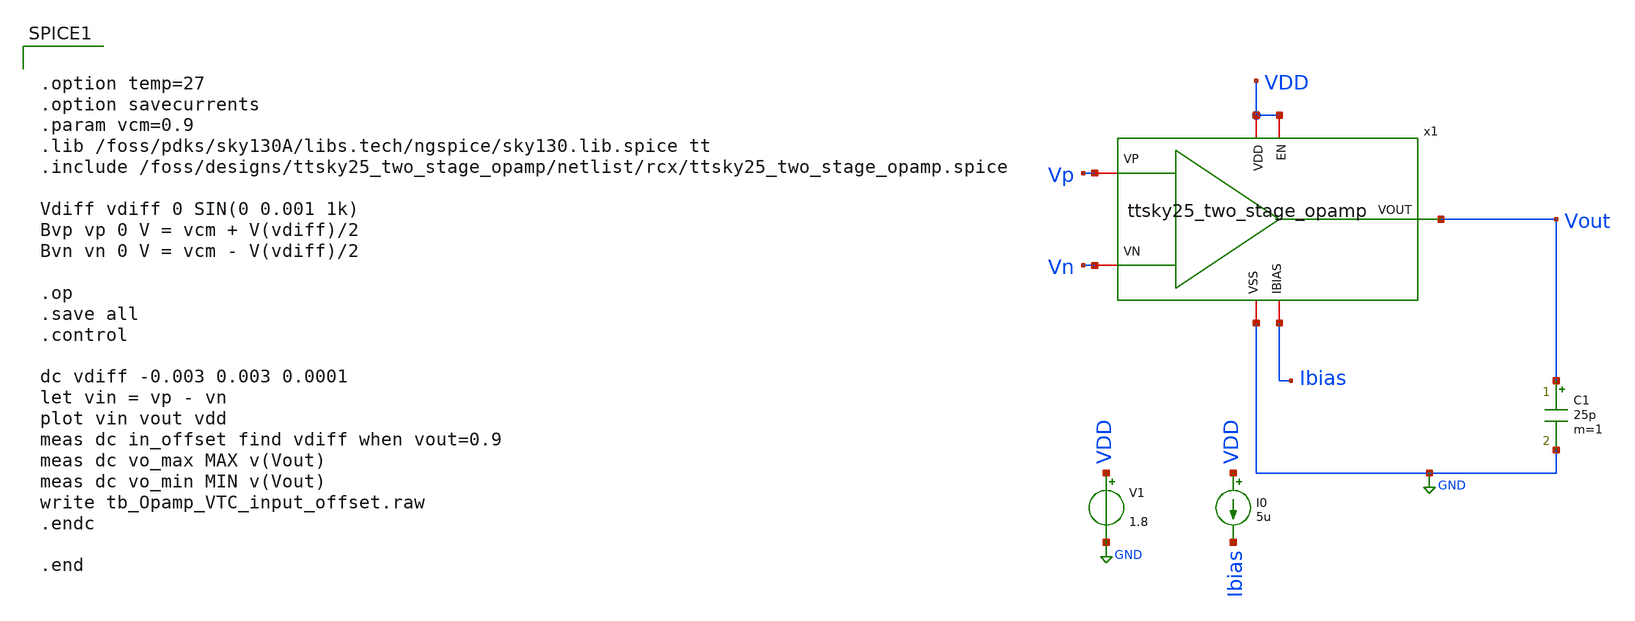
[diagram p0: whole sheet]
** sch_path: xschem/post-layout/testbenches/tb_Opamp_VTC_input_offset.sch
**.subckt tb_Opamp_VTC_input_offset
V1 VDD GND 1.8
I0 VDD Ibias 5u
C1 Vout GND 25p m=1
x1 VDD Ibias Vout Vn Vp VDD GND ttsky25_two_stage_opamp
**** begin user architecture code


.option temp=27
.option savecurrents
.param vcm=0.9
.lib /foss/pdks/sky130A/libs.tech/ngspice/sky130.lib.spice tt
.include /foss/designs/ttsky25_two_stage_opamp/netlist/rcx/ttsky25_two_stage_opamp.spice

Vdiff vdiff 0 SIN(0 0.001 1k)
Bvp vp 0 V = vcm + V(vdiff)/2
Bvn vn 0 V = vcm - V(vdiff)/2

.op
.save all
.control

dc vdiff -0.003 0.003 0.0001
let vin = vp - vn
plot vin vout vdd
meas dc in_offset find vdiff when vout=0.9
meas dc vo_max MAX v(Vout)
meas dc vo_min MIN v(Vout)
write tb_Opamp_VTC_input_offset.raw
.endc

.end


**** end user architecture code
**.ends
.GLOBAL GND
.end
